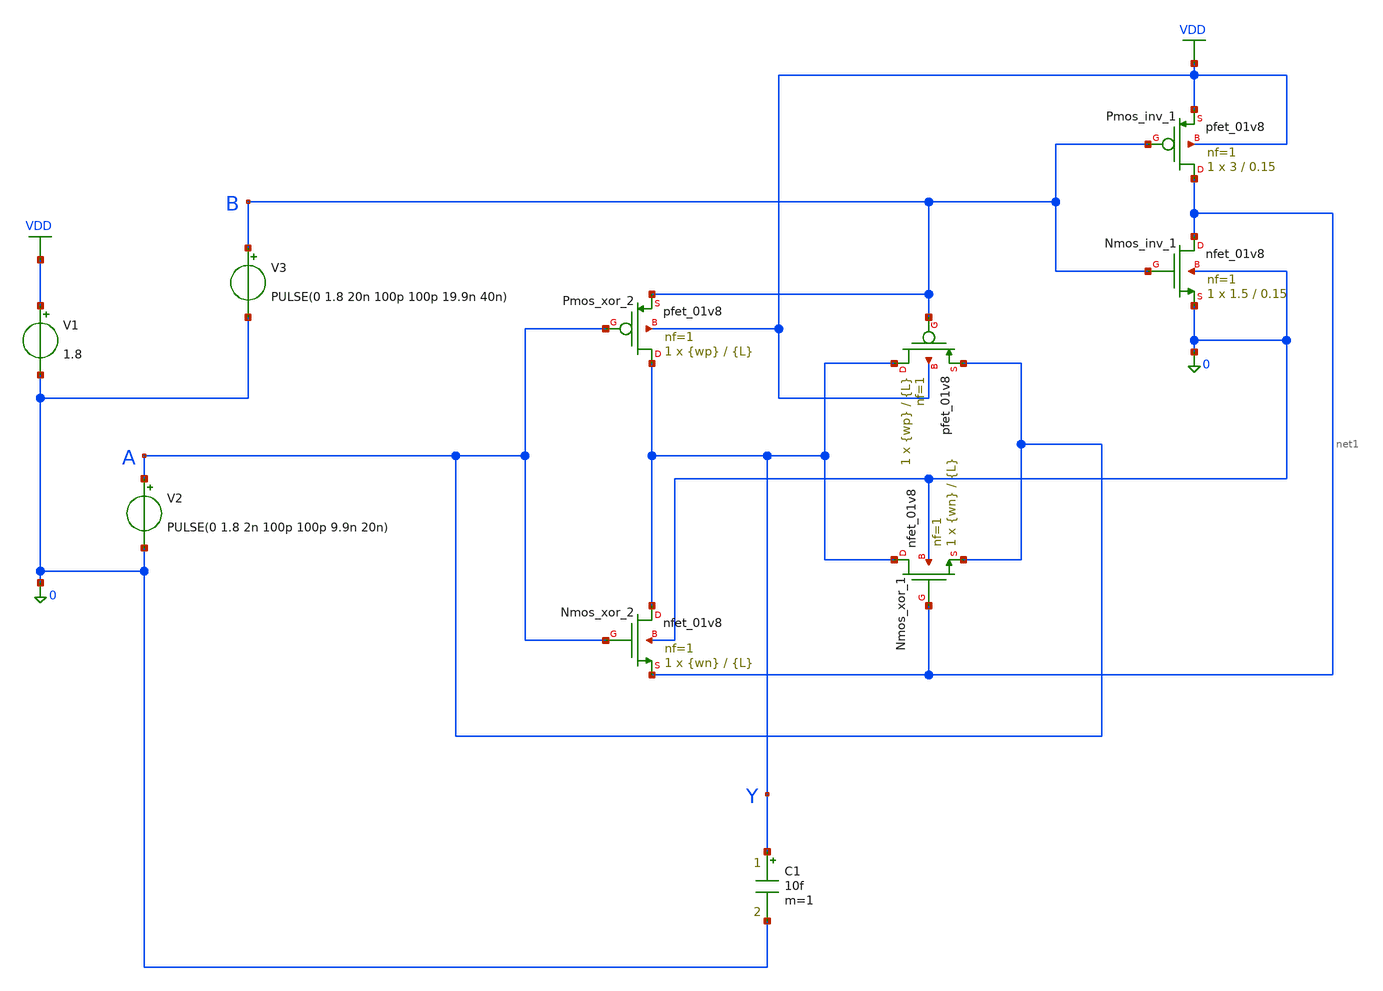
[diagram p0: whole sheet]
** sch_path: cells/full_adder_tg/xschem/test_xor2_design_khaosat.sch
**.subckt test_xor2_design_khaosat
XPmos_inv_1 net1 B VDD VDD sky130_fd_pr__pfet_01v8 L=0.15 W=3 nf=1 ad='int((1 + 1)/2) * 3 / 1 * 0.29'
+ as='int((1 + 2)/2) * 3 / 1 * 0.29' pd='2*int((1 + 1)/2) * (3 / 1 + 0.29)' ps='2*int((1 + 2)/2) * (3 / 1 + 0.29)'
+ nrd='0.29 / 3 ' nrs='0.29 / 3 ' sa=0 sb=0 sd=0 mult=1 m=1
XNmos_inv_1 net1 B 0 0 sky130_fd_pr__nfet_01v8 L=0.15 W=1.5 nf=1 ad='int((1 + 1)/2) * 1.5 / 1 * 0.29'
+ as='int((1 + 2)/2) * 1.5 / 1 * 0.29' pd='2*int((1 + 1)/2) * (1.5 / 1 + 0.29)' ps='2*int((1 + 2)/2) * (1.5 / 1 + 0.29)'
+ nrd='0.29 / 1.5 ' nrs='0.29 / 1.5 ' sa=0 sb=0 sd=0 mult=1 m=1
XM1 Y B A VDD sky130_fd_pr__pfet_01v8 L={L} W={wp} nf=1 ad='int((1 + 1)/2) * {wp} / 1 * 0.29' as='int((1 + 2)/2) * {wp} / 1 * 0.29'
+ pd='2*int((1 + 1)/2) * ({wp} / 1 + 0.29)' ps='2*int((1 + 2)/2) * ({wp} / 1 + 0.29)' nrd='0.29 / {wp} '
+ nrs='0.29 / {wp} ' sa=0 sb=0 sd=0 mult=1 m=1
XNmos_xor_1 Y net1 A 0 sky130_fd_pr__nfet_01v8 L={L} W={wn} nf=1 ad='int((1 + 1)/2) * {wn} / 1 * 0.29'
+ as='int((1 + 2)/2) * {wn} / 1 * 0.29' pd='2*int((1 + 1)/2) * ({wn} / 1 + 0.29)' ps='2*int((1 + 2)/2) * ({wn} / 1 + 0.29)'
+ nrd='0.29 / {wn} ' nrs='0.29 / {wn} ' sa=0 sb=0 sd=0 mult=1 m=1
XPmos_xor_2 Y A B VDD sky130_fd_pr__pfet_01v8 L={L} W={wp} nf=1 ad='int((1 + 1)/2) * {wp} / 1 * 0.29'
+ as='int((1 + 2)/2) * {wp} / 1 * 0.29' pd='2*int((1 + 1)/2) * ({wp} / 1 + 0.29)' ps='2*int((1 + 2)/2) * ({wp} / 1 + 0.29)'
+ nrd='0.29 / {wp} ' nrs='0.29 / {wp} ' sa=0 sb=0 sd=0 mult=1 m=1
XNmos_xor_2 Y A net1 0 sky130_fd_pr__nfet_01v8 L={L} W={wn} nf=1 ad='int((1 + 1)/2) * {wn} / 1 * 0.29'
+ as='int((1 + 2)/2) * {wn} / 1 * 0.29' pd='2*int((1 + 1)/2) * ({wn} / 1 + 0.29)' ps='2*int((1 + 2)/2) * ({wn} / 1 + 0.29)'
+ nrd='0.29 / {wn} ' nrs='0.29 / {wn} ' sa=0 sb=0 sd=0 mult=1 m=1
V1 VDD 0 1.8
V2 A 0 PULSE(0 1.8 2n 100p 100p 9.9n 20n)
V3 B 0 PULSE(0 1.8 20n 100p 100p 19.9n 40n)
C1 Y 0 10f m=1
**.ends
.GLOBAL VDD
**** begin user architecture code

.lib /foss/pdks/sky130A/libs.tech/ngspice/sky130.lib.spice tt
.temp 27
.param L=0.15
.param wn=2.0
.param wp=4.0

.control
echo "L_um | tplh_ps | tphl_ps | tpd_ps | Pavg_uW | PDP_fJ"
foreach l_val 0.15 0.18 0.20 0.25 0.30
  alterparam L = $l_val
  reset
  tran 5p 40n

  meas tran tplh TRIG v(A) VAL=0.9 RISE=1 TARG v(Y) VAL=0.9 RISE=1
  meas tran tphl TRIG v(A) VAL=0.9 FALL=1 TARG v(Y) VAL=0.9 FALL=1
  meas tran iavg AVG i(V1) FROM=0 TO=40n

  let tplh_ps = tplh * 1e12
  let tphl_ps = tphl * 1e12
  let tpd_ps  = (tplh + tphl) / 2 * 1e12
  let pavg_uw = abs(1.8 * iavg) * 1e6
  let pdp_fj  = tpd_ps * pavg_uw * 1e-3

  echo "$l_val | $&tplh_ps | $&tphl_ps | $&tpd_ps | $&pavg_uw | $&pdp_fj"
end
write test_xor2_design_khaosat.raw v(A) v(B) v(Y)
.endc

**** end user architecture code
.end
